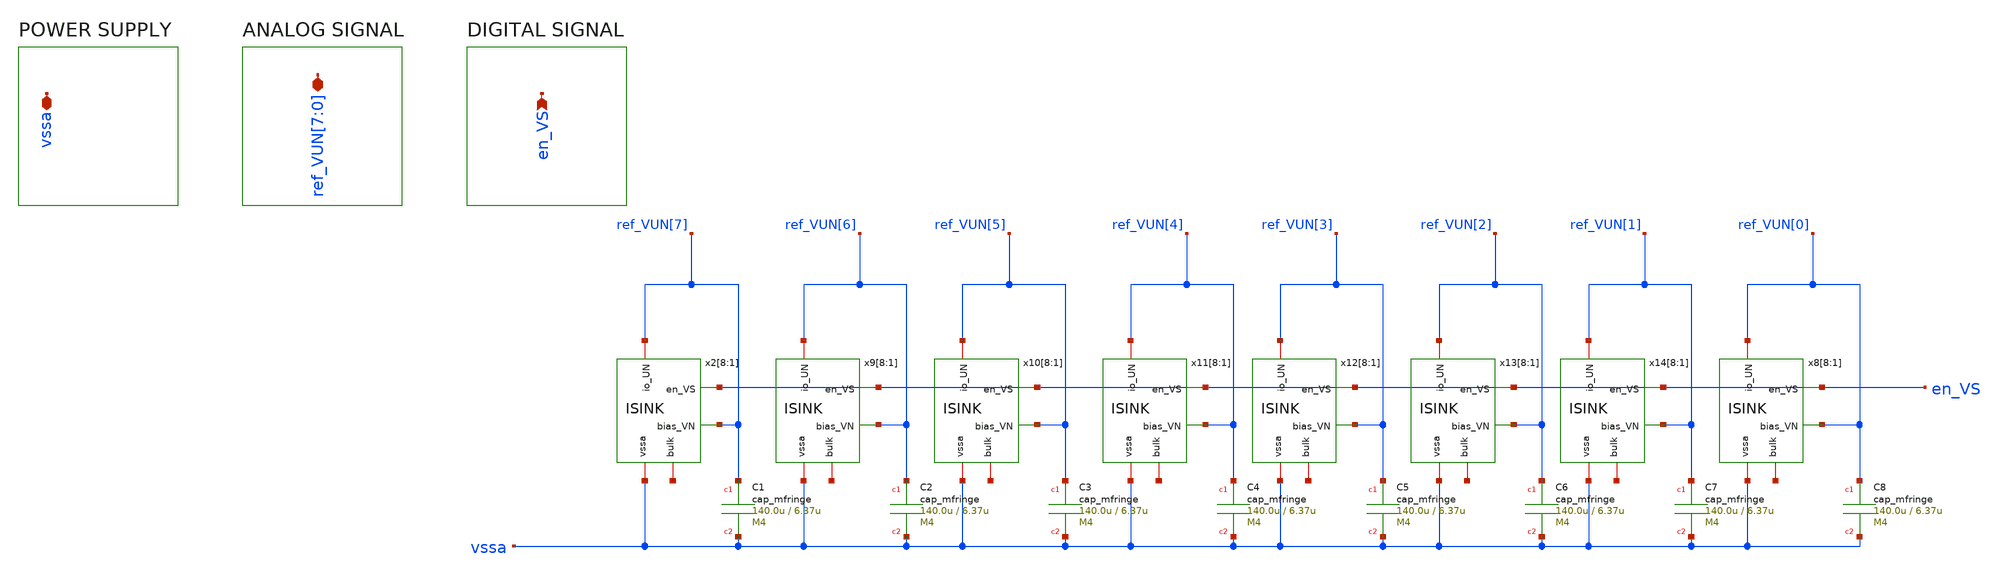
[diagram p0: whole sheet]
** sch_path: CoreDiodeT.sch
**.subckt CoreDiodeT
*+ ref_VUN[7],ref_VUN[6],ref_VUN[5],ref_VUN[4],ref_VUN[3],ref_VUN[2],ref_VUN[1],ref_VUN[0] en_VS vssa
*.iopin ref_VUN[7],ref_VUN[6],ref_VUN[5],ref_VUN[4],ref_VUN[3],ref_VUN[2],ref_VUN[1],ref_VUN[0]
*.ipin en_VS
*.iopin vssa
x2[8] ref_VUN[7] vssa en_VS ref_VUN[7] net1[7] ISINK
x2[7] ref_VUN[7] vssa en_VS ref_VUN[7] net1[6] ISINK
x2[6] ref_VUN[7] vssa en_VS ref_VUN[7] net1[5] ISINK
x2[5] ref_VUN[7] vssa en_VS ref_VUN[7] net1[4] ISINK
x2[4] ref_VUN[7] vssa en_VS ref_VUN[7] net1[3] ISINK
x2[3] ref_VUN[7] vssa en_VS ref_VUN[7] net1[2] ISINK
x2[2] ref_VUN[7] vssa en_VS ref_VUN[7] net1[1] ISINK
x2[1] ref_VUN[7] vssa en_VS ref_VUN[7] net1[0] ISINK
x9[8] ref_VUN[6] vssa en_VS ref_VUN[6] net2[7] ISINK
x9[7] ref_VUN[6] vssa en_VS ref_VUN[6] net2[6] ISINK
x9[6] ref_VUN[6] vssa en_VS ref_VUN[6] net2[5] ISINK
x9[5] ref_VUN[6] vssa en_VS ref_VUN[6] net2[4] ISINK
x9[4] ref_VUN[6] vssa en_VS ref_VUN[6] net2[3] ISINK
x9[3] ref_VUN[6] vssa en_VS ref_VUN[6] net2[2] ISINK
x9[2] ref_VUN[6] vssa en_VS ref_VUN[6] net2[1] ISINK
x9[1] ref_VUN[6] vssa en_VS ref_VUN[6] net2[0] ISINK
x10[8] ref_VUN[5] vssa en_VS ref_VUN[5] net3[7] ISINK
x10[7] ref_VUN[5] vssa en_VS ref_VUN[5] net3[6] ISINK
x10[6] ref_VUN[5] vssa en_VS ref_VUN[5] net3[5] ISINK
x10[5] ref_VUN[5] vssa en_VS ref_VUN[5] net3[4] ISINK
x10[4] ref_VUN[5] vssa en_VS ref_VUN[5] net3[3] ISINK
x10[3] ref_VUN[5] vssa en_VS ref_VUN[5] net3[2] ISINK
x10[2] ref_VUN[5] vssa en_VS ref_VUN[5] net3[1] ISINK
x10[1] ref_VUN[5] vssa en_VS ref_VUN[5] net3[0] ISINK
x11[8] ref_VUN[4] vssa en_VS ref_VUN[4] net4[7] ISINK
x11[7] ref_VUN[4] vssa en_VS ref_VUN[4] net4[6] ISINK
x11[6] ref_VUN[4] vssa en_VS ref_VUN[4] net4[5] ISINK
x11[5] ref_VUN[4] vssa en_VS ref_VUN[4] net4[4] ISINK
x11[4] ref_VUN[4] vssa en_VS ref_VUN[4] net4[3] ISINK
x11[3] ref_VUN[4] vssa en_VS ref_VUN[4] net4[2] ISINK
x11[2] ref_VUN[4] vssa en_VS ref_VUN[4] net4[1] ISINK
x11[1] ref_VUN[4] vssa en_VS ref_VUN[4] net4[0] ISINK
x12[8] ref_VUN[3] vssa en_VS ref_VUN[3] net5[7] ISINK
x12[7] ref_VUN[3] vssa en_VS ref_VUN[3] net5[6] ISINK
x12[6] ref_VUN[3] vssa en_VS ref_VUN[3] net5[5] ISINK
x12[5] ref_VUN[3] vssa en_VS ref_VUN[3] net5[4] ISINK
x12[4] ref_VUN[3] vssa en_VS ref_VUN[3] net5[3] ISINK
x12[3] ref_VUN[3] vssa en_VS ref_VUN[3] net5[2] ISINK
x12[2] ref_VUN[3] vssa en_VS ref_VUN[3] net5[1] ISINK
x12[1] ref_VUN[3] vssa en_VS ref_VUN[3] net5[0] ISINK
x13[8] ref_VUN[2] vssa en_VS ref_VUN[2] net6[7] ISINK
x13[7] ref_VUN[2] vssa en_VS ref_VUN[2] net6[6] ISINK
x13[6] ref_VUN[2] vssa en_VS ref_VUN[2] net6[5] ISINK
x13[5] ref_VUN[2] vssa en_VS ref_VUN[2] net6[4] ISINK
x13[4] ref_VUN[2] vssa en_VS ref_VUN[2] net6[3] ISINK
x13[3] ref_VUN[2] vssa en_VS ref_VUN[2] net6[2] ISINK
x13[2] ref_VUN[2] vssa en_VS ref_VUN[2] net6[1] ISINK
x13[1] ref_VUN[2] vssa en_VS ref_VUN[2] net6[0] ISINK
x14[8] ref_VUN[1] vssa en_VS ref_VUN[1] net7[7] ISINK
x14[7] ref_VUN[1] vssa en_VS ref_VUN[1] net7[6] ISINK
x14[6] ref_VUN[1] vssa en_VS ref_VUN[1] net7[5] ISINK
x14[5] ref_VUN[1] vssa en_VS ref_VUN[1] net7[4] ISINK
x14[4] ref_VUN[1] vssa en_VS ref_VUN[1] net7[3] ISINK
x14[3] ref_VUN[1] vssa en_VS ref_VUN[1] net7[2] ISINK
x14[2] ref_VUN[1] vssa en_VS ref_VUN[1] net7[1] ISINK
x14[1] ref_VUN[1] vssa en_VS ref_VUN[1] net7[0] ISINK
x8[8] ref_VUN[0] vssa en_VS ref_VUN[0] net8[7] ISINK
x8[7] ref_VUN[0] vssa en_VS ref_VUN[0] net8[6] ISINK
x8[6] ref_VUN[0] vssa en_VS ref_VUN[0] net8[5] ISINK
x8[5] ref_VUN[0] vssa en_VS ref_VUN[0] net8[4] ISINK
x8[4] ref_VUN[0] vssa en_VS ref_VUN[0] net8[3] ISINK
x8[3] ref_VUN[0] vssa en_VS ref_VUN[0] net8[2] ISINK
x8[2] ref_VUN[0] vssa en_VS ref_VUN[0] net8[1] ISINK
x8[1] ref_VUN[0] vssa en_VS ref_VUN[0] net8[0] ISINK
XC1 ref_VUN[7] vssa cap_mfringe w=140.0u l=6.37u mmin=1 mmax=4
XC2 ref_VUN[6] vssa cap_mfringe w=140.0u l=6.37u mmin=1 mmax=4
XC3 ref_VUN[5] vssa cap_mfringe w=140.0u l=6.37u mmin=1 mmax=4
XC4 ref_VUN[4] vssa cap_mfringe w=140.0u l=6.37u mmin=1 mmax=4
XC5 ref_VUN[3] vssa cap_mfringe w=140.0u l=6.37u mmin=1 mmax=4
XC6 ref_VUN[2] vssa cap_mfringe w=140.0u l=6.37u mmin=1 mmax=4
XC7 ref_VUN[1] vssa cap_mfringe w=140.0u l=6.37u mmin=1 mmax=4
XC8 ref_VUN[0] vssa cap_mfringe w=140.0u l=6.37u mmin=1 mmax=4
**.ends

* expanding   symbol:  ISINK.sym # of pins=5
** sym_path: ISINK.sym
** sch_path: ISINK.sch
.subckt ISINK bias_VN vssa en_VS io_UN bulk
*.ipin en_VS
*.iopin vssa
*.ipin bias_VN
*.iopin io_UN
*.iopin bulk
XM1 io_UN en_VS net2 bulk sg13_hv_nmos w=2.5u l=0.5u ng=1 m=1 mm_ok=1
XM2 net2 bias_VN net1 bulk sg13_hv_nmos w=1u l=4u ng=1 m=1 mm_ok=1
XM3 net1 bias_VN vssa bulk sg13_hv_nmos w=1u l=4u ng=1 m=1 mm_ok=1
.ends

.end
